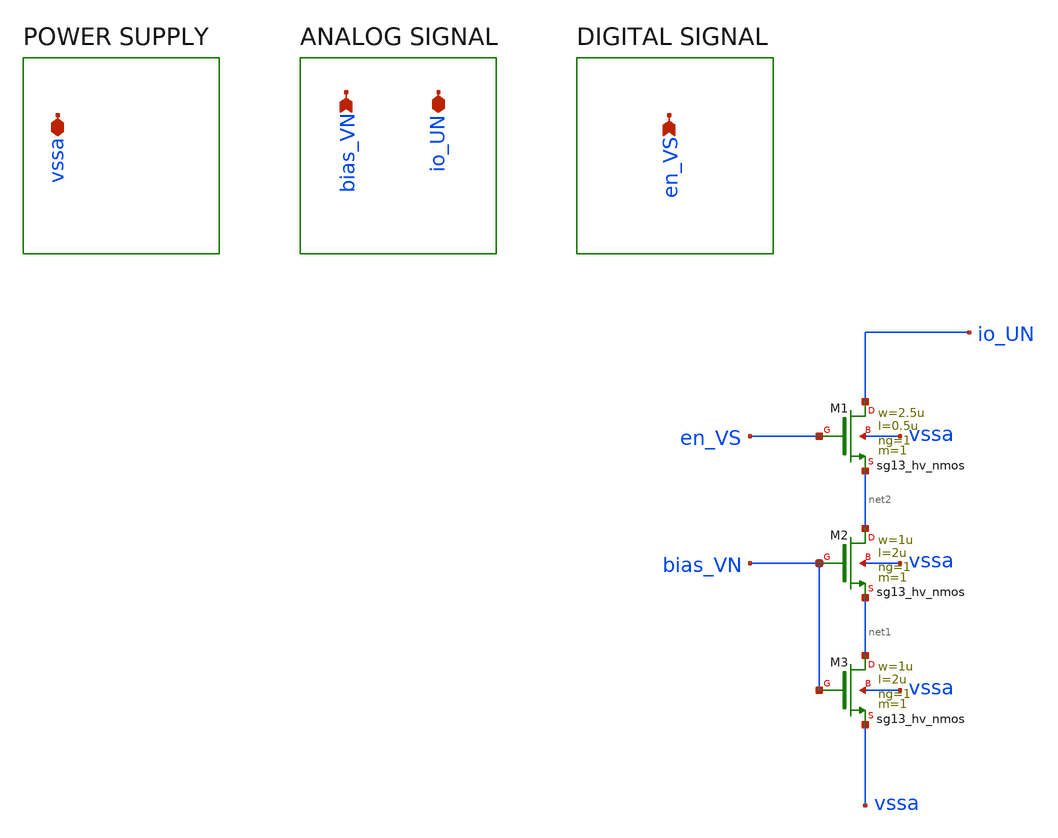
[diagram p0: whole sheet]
** sch_path: ISINK.sch
**.subckt ISINK en_VS vssa bias_VN io_UN
*.ipin en_VS
*.iopin vssa
*.ipin bias_VN
*.iopin io_UN
XM1 io_UN en_VS net2 vssa sg13_hv_nmos w=2.5u l=0.5u ng=1 m=1 mm_ok=1
XM2 net2 bias_VN net1 vssa sg13_hv_nmos w=1u l=2u ng=1 m=1 mm_ok=1
XM3 net1 bias_VN vssa vssa sg13_hv_nmos w=1u l=2u ng=1 m=1 mm_ok=1
**.ends
.end
